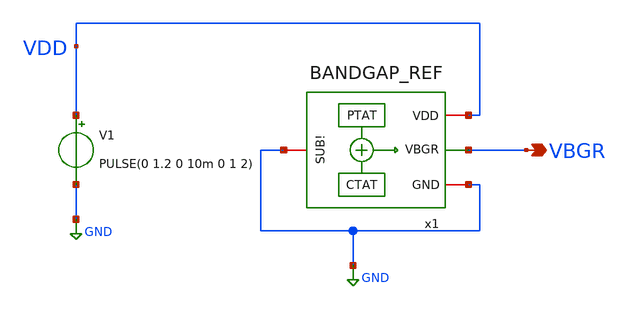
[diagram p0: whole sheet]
** sch_path: xschem/bgr/tb_BGR.sch
**.subckt tb_BGR VBGR
*.opin VBGR
V1 VDD GND PULSE(0 1.2 0 10m 0 1 2)
x1 VDD GND VBGR GND BANDGAP_REF
**** begin user architecture code



.option rshunt=1.0e12
.control
save all
save VDD
alter V1 dc 1.2

op
print I(Vmeas)
print v(VBGR)
print -i(V1)

dc TEMP 100 -50 -5
print I(Vmeas)
print v(VBGR)
plot v(VBGR)

write tb_BGR_temp.raw
.endc

.control
save all
tran 100u 15m

print I(Vmeas)
meas tran vb_end find v(VBGR) at=15m
meas tran vb_max max v(VBGR) from=5m to=15m
meas tran vb_min min v(VBGR) from=5m to=15m
* supply current (negative = drawn from the source), power = 1.2 V x |idd|
meas tran idd avg i(V1) from=13m to=15m
plot v(VBGR)

write tb_BGR_transient.raw
.endc




.lib cornerMOSlv.lib mos_tt
.lib cornerMOShv.lib mos_tt
.lib cornerRES.lib res_typ
.lib cornerCAP.lib cap_typ

**** end user architecture code
**.ends

* expanding   symbol:  xschem/bgr/BANDGAP_REF.sym # of pins=4
** sym_path: xschem/bgr/BANDGAP_REF.sym
** sch_path: xschem/bgr/BANDGAP_REF.sch
.subckt BANDGAP_REF VDD GND VBGR SUB!
*.opin VBGR
*.iopin GND
*.iopin VDD
*.iopin SUB!
XM8 GND v- net1 SUB! sg13_lv_nmos w=150n l=10u ng=1 m=1 mm_ok=1
XM6 net1 net1 VDD bulk6 sg13_lv_pmos w=1u l=1u ng=1 m=1 mm_ok=1
XM7 net2 net1 VDD bulk6 sg13_lv_pmos w=1u l=1u ng=1 m=1 mm_ok=1
XM9 v- net2 VDD bulk5 sg13_lv_pmos w=200n l=4u ng=1 m=1 mm_ok=1
XM1 v- v+ GND SUB! sg13_lv_nmos w=7.14u l=5u ng=4 m=1 mm_ok=1
XM2 net3 net3 GND SUB! sg13_lv_nmos w=21u l=5u ng=8 m=1 mm_ok=1
XM3 v- Vo1 VDD bulk7 sg13_lv_pmos w=15u l=5u ng=8 m=1 mm_ok=1
XM4 v+ Vo1 VDD bulk7 sg13_lv_pmos w=15u l=5u ng=8 m=1 mm_ok=1
XM5 VBGR Vo1 VDD bulk7 sg13_lv_pmos w=16u l=5u ng=8 m=1 mm_ok=1
XR2 VBGR net11 sub! rppd w=0.710e-6 l=38.65e-6 m=1 b=0 mm_ok=1
XC1 net2 GND cap_cmim w=18.2e-6 l=18.2e-6 m=1 mm_ok=1
XM10 dn3 v- dn2 bulk sg13_lv_pmos w=3.64u l=3.7u ng=1 m=2 mm_ok=1
XM11 dn4 v+ dn2 bulk sg13_lv_pmos w=3.64u l=3.7u ng=1 m=2 mm_ok=1
XM12 dn4 VDD VDD bulk sg13_lv_pmos w=3.64u l=3.7u ng=1 m=2 mm_ok=1
XM13 dn3 VDD VDD bulk sg13_lv_pmos w=3.64u l=3.7u ng=1 m=2 mm_ok=1
XM15 dn2 VDD VDD bulk sg13_lv_pmos w=3.64u l=3.7u ng=1 m=2 mm_ok=1
XM16 dn2 VDD VDD bulk sg13_lv_pmos w=3.64u l=3.7u ng=1 m=2 mm_ok=1
XR4 VDD bulk ntap1 R=2.445 w=33.53e-6 l=13.15e-6 rw=0.36e-6
XM14 dn2 iout VDD bulk1 sg13_lv_pmos w=5.3u l=1.95u ng=1 m=1 mm_ok=1
XR5 GND SUB! ptap1 R=6.689 w=12.57e-6 l=4.39e-6 rw=0.72e-6
XR6 VDD bulk1 ntap1 R=7.319 w=6.765e-6 l=8.86e-6 rw=0.72e-6
XM17 GND dn3 dn3 SUB! sg13_lv_nmos w=720n l=9.75u ng=1 m=1 mm_ok=1
XM18 GND dn3 dn4 SUB! sg13_lv_nmos w=720n l=9.75u ng=1 m=1 mm_ok=1
XM19 Vo1 iout VDD bulk4 sg13_lv_pmos w=75u l=2.08u ng=8 m=1 mm_ok=1
XM20 GND dn4 Vo1 SUB! sg13_lv_nmos w=28.8u l=9.75u ng=4 m=1 mm_ok=1
XM21 iout iout VDD bulk4 sg13_lv_pmos w=75u l=2.08u ng=8 m=1 mm_ok=1
XC2 dn4 Vo1 cap_cmim w=22.29e-6 l=22.29e-6 m=1 mm_ok=1
XR8 VDD bulk4 ntap1 R=2.291 w=23.54e-6 l=23.22e-6 rw=0.72e-6
XR9 VDD bulk6 ntap1 R=7.123 w=5.76e-6 l=10.255e-6 rw=0.72e-6
XR12 v+ net7 sub! rppd w=0.5e-6 l=38.65e-6 m=1 b=0 mm_ok=1
XR3 net7 net6 sub! rppd w=0.5e-6 l=38.65e-6 m=1 b=0 mm_ok=1
XR13 net6 net5 sub! rppd w=0.5e-6 l=38.65e-6 m=1 b=0 mm_ok=1
XR14 net5 net4 sub! rppd w=0.5e-6 l=38.65e-6 m=1 b=0 mm_ok=1
XR15 net4 net3 sub! rppd w=0.5e-6 l=38.65e-6 m=1 b=0 mm_ok=1
XR16 net10 net9 sub! rppd w=0.5e-6 l=38.65e-6 m=1 b=0 mm_ok=1
XR17 net9 net8 sub! rppd w=0.5e-6 l=38.65e-6 m=1 b=0 mm_ok=1
XR18 net8 net17 sub! rppd w=0.5e-6 l=38.65e-6 m=1 b=0 mm_ok=1
XR19 net17 GND sub! rppd w=3e-6 l=38.65e-6 m=1 b=0 mm_ok=1
XR20 net11 net12 sub! rppd w=0.710e-6 l=38.65e-6 m=1 b=0 mm_ok=1
XR21 net12 net13 sub! rppd w=0.710e-6 l=38.65e-6 m=1 b=0 mm_ok=1
XR22 net13 net14 sub! rppd w=0.710e-6 l=38.65e-6 m=1 b=0 mm_ok=1
XR23 net14 net15 sub! rppd w=0.710e-6 l=38.65e-6 m=1 b=0 mm_ok=1
XR24 net15 net16 sub! rppd w=0.710e-6 l=38.65e-6 m=1 b=0 mm_ok=1
XR25 net16 GND sub! rppd w=0.710e-6 l=38.65e-6 m=1 b=0 mm_ok=1
XR26 VDD bulk5 ntap1 R=11.59 w=7.37e-6 l=3.03e-6 rw=0.72e-6
XR27 VDD bulk7 ntap1 R=1.868 w=46.185e-6 l=10.815e-6 rw=0.72e-6
XR7 GND SUB! ptap1 R=7.306 w=2.73e-6 l=12.92e-6 rw=0.72e-6
XR10 GND SUB! ptap1 R=2.076 w=46.215e-6 l=5.225e-6 rw=0.72e-6
XR11 GND SUB! ptap1 R=3.763 w=4.985e-6 l=24.045e-6 rw=0.72e-6
XR28 GND SUB! ptap1 R=2.219 w=9.24e-6 l=42.505e-6 rw=0.32e-6
XC3 VDD GND cap_cmim w=5e-6 l=5e-6 m=15 mm_ok=1
XR31 v+ net10 sub! rppd w=0.5e-6 l=38.65e-6 m=1 b=0 mm_ok=1
XR1 iout GND sub! rppd w=0.5e-6 l=15e-6 m=1 b=0 mm_ok=1
.ends

.GLOBAL GND
.GLOBAL VDD
.end
